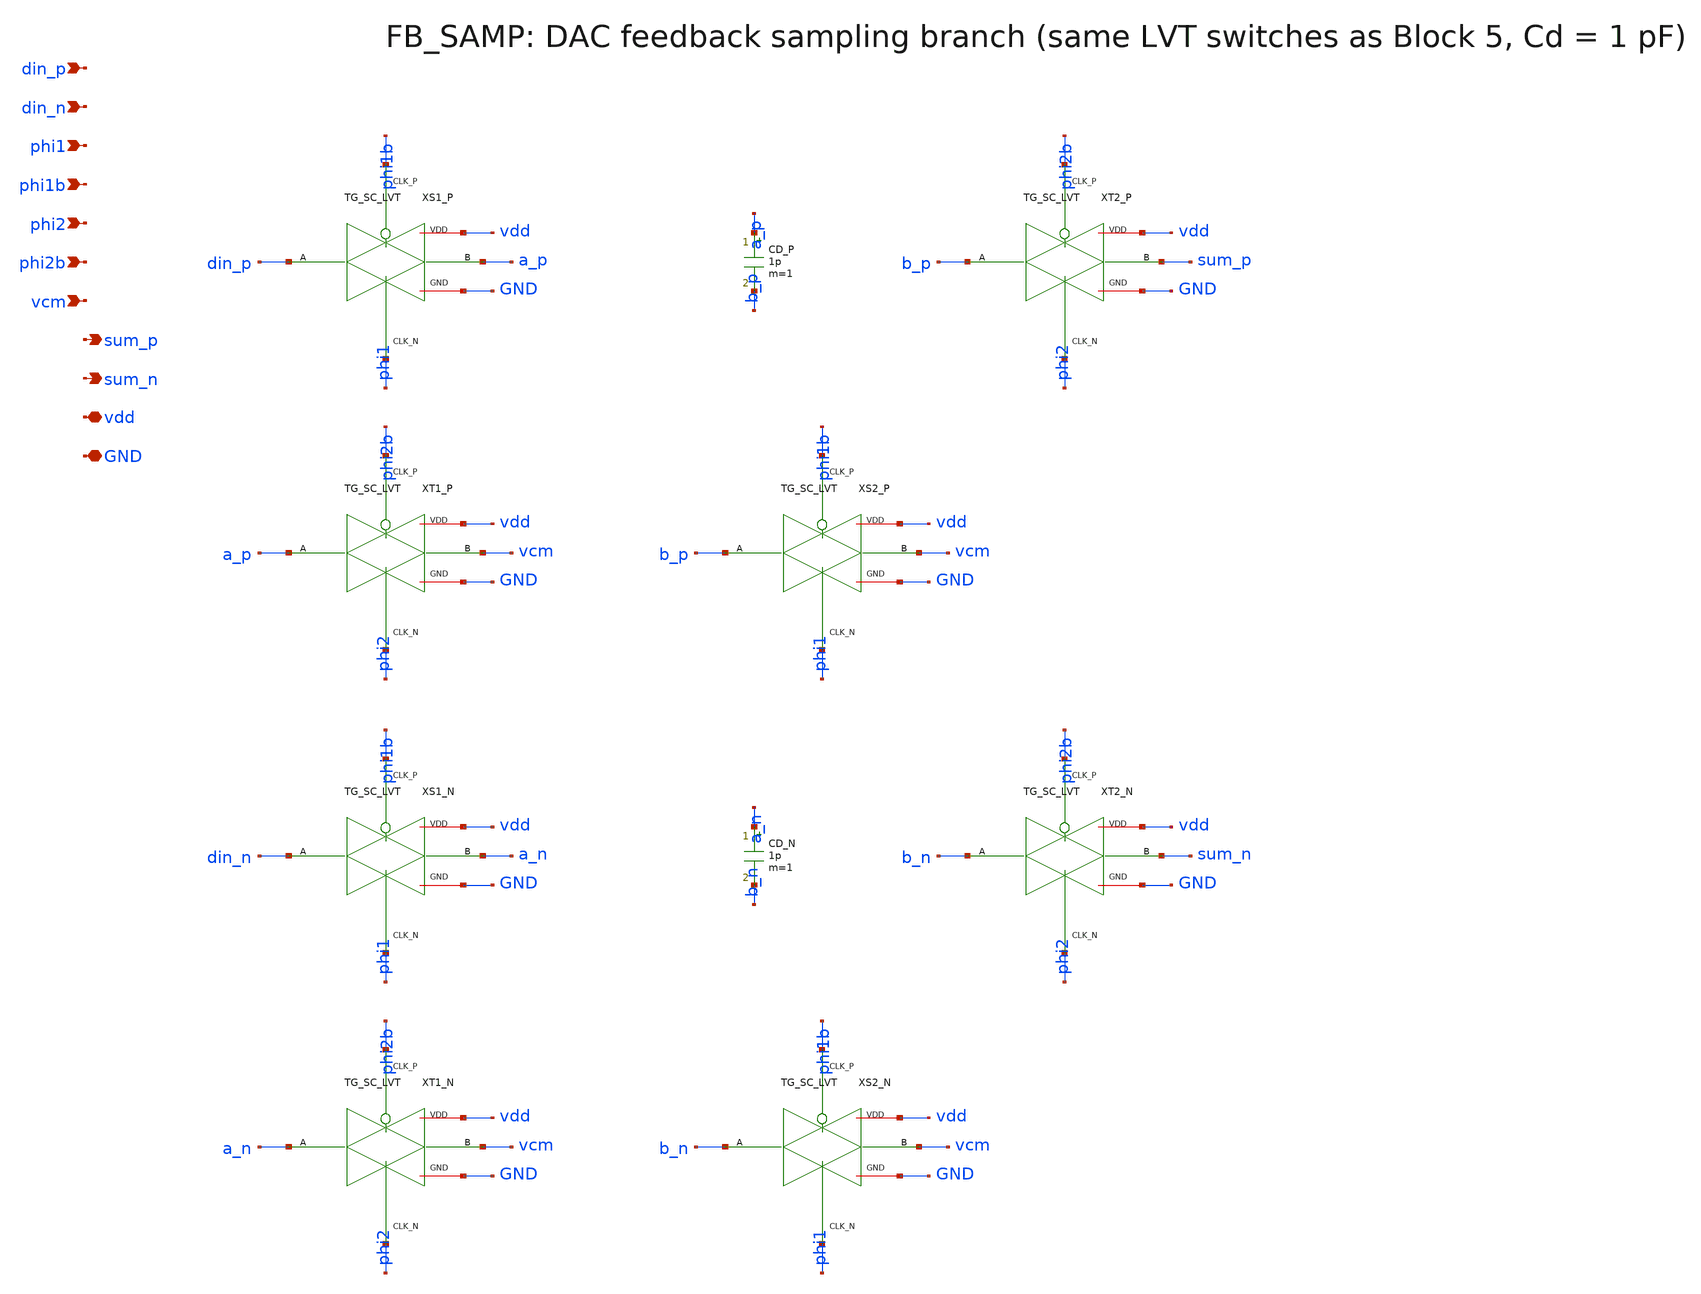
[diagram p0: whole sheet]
** sch_path: top_level/xschem/FB_SAMP.sch
**.subckt FB_SAMP din_p din_n phi1 phi1b phi2 phi2b vcm sum_p sum_n vdd GND
*.ipin din_p
*.ipin din_n
*.ipin phi1
*.ipin phi1b
*.ipin phi2
*.ipin phi2b
*.ipin vcm
*.opin sum_p
*.opin sum_n
*.iopin vdd
*.iopin GND
XS1_P din_p a_p phi1b phi1 vdd GND TG_SC_LVT
XT2_P b_p sum_p phi2b phi2 vdd GND TG_SC_LVT
CD_P a_p b_p 1p m=1
XT1_P a_p vcm phi2b phi2 vdd GND TG_SC_LVT
XS2_P b_p vcm phi1b phi1 vdd GND TG_SC_LVT
XS1_N din_n a_n phi1b phi1 vdd GND TG_SC_LVT
XT2_N b_n sum_n phi2b phi2 vdd GND TG_SC_LVT
CD_N a_n b_n 1p m=1
XT1_N a_n vcm phi2b phi2 vdd GND TG_SC_LVT
XS2_N b_n vcm phi1b phi1 vdd GND TG_SC_LVT
**.ends

* expanding   symbol:  blocks/05_Switch_Network/xschem/TG_SC_LVT.sym # of pins=6
** sym_path: blocks/05_Switch_Network/xschem/TG_SC_LVT.sym
** sch_path: blocks/05_Switch_Network/xschem/TG_SC_LVT.sch
.subckt TG_SC_LVT A B CLK_P CLK_N VDD GND
*.iopin A
*.iopin B
*.ipin CLK_P
*.ipin CLK_N
*.iopin VDD
*.iopin GND
XMP A CLK_P B VDD sky130_fd_pr__pfet_01v8_lvt L=0.35 W=8 nf=1 ad='int((1 + 1)/2) * 8 / 1 * 0.29' as='int((1 + 2)/2) * 8 / 1 * 0.29'
+ pd='2*int((1 + 1)/2) * (8 / 1 + 0.29)' ps='2*int((1 + 2)/2) * (8 / 1 + 0.29)' nrd='0.29 / 8 ' nrs='0.29 / 8 '
+ sa=0 sb=0 sd=0 mult=1
XMN A CLK_N B GND sky130_fd_pr__nfet_01v8_lvt L=0.15 W=4 nf=1 ad='int((1 + 1)/2) * 4 / 1 * 0.29' as='int((1 + 2)/2) * 4 / 1 * 0.29'
+ pd='2*int((1 + 1)/2) * (4 / 1 + 0.29)' ps='2*int((1 + 2)/2) * (4 / 1 + 0.29)' nrd='0.29 / 4 ' nrs='0.29 / 4 '
+ sa=0 sb=0 sd=0 mult=1
.ends

.end
